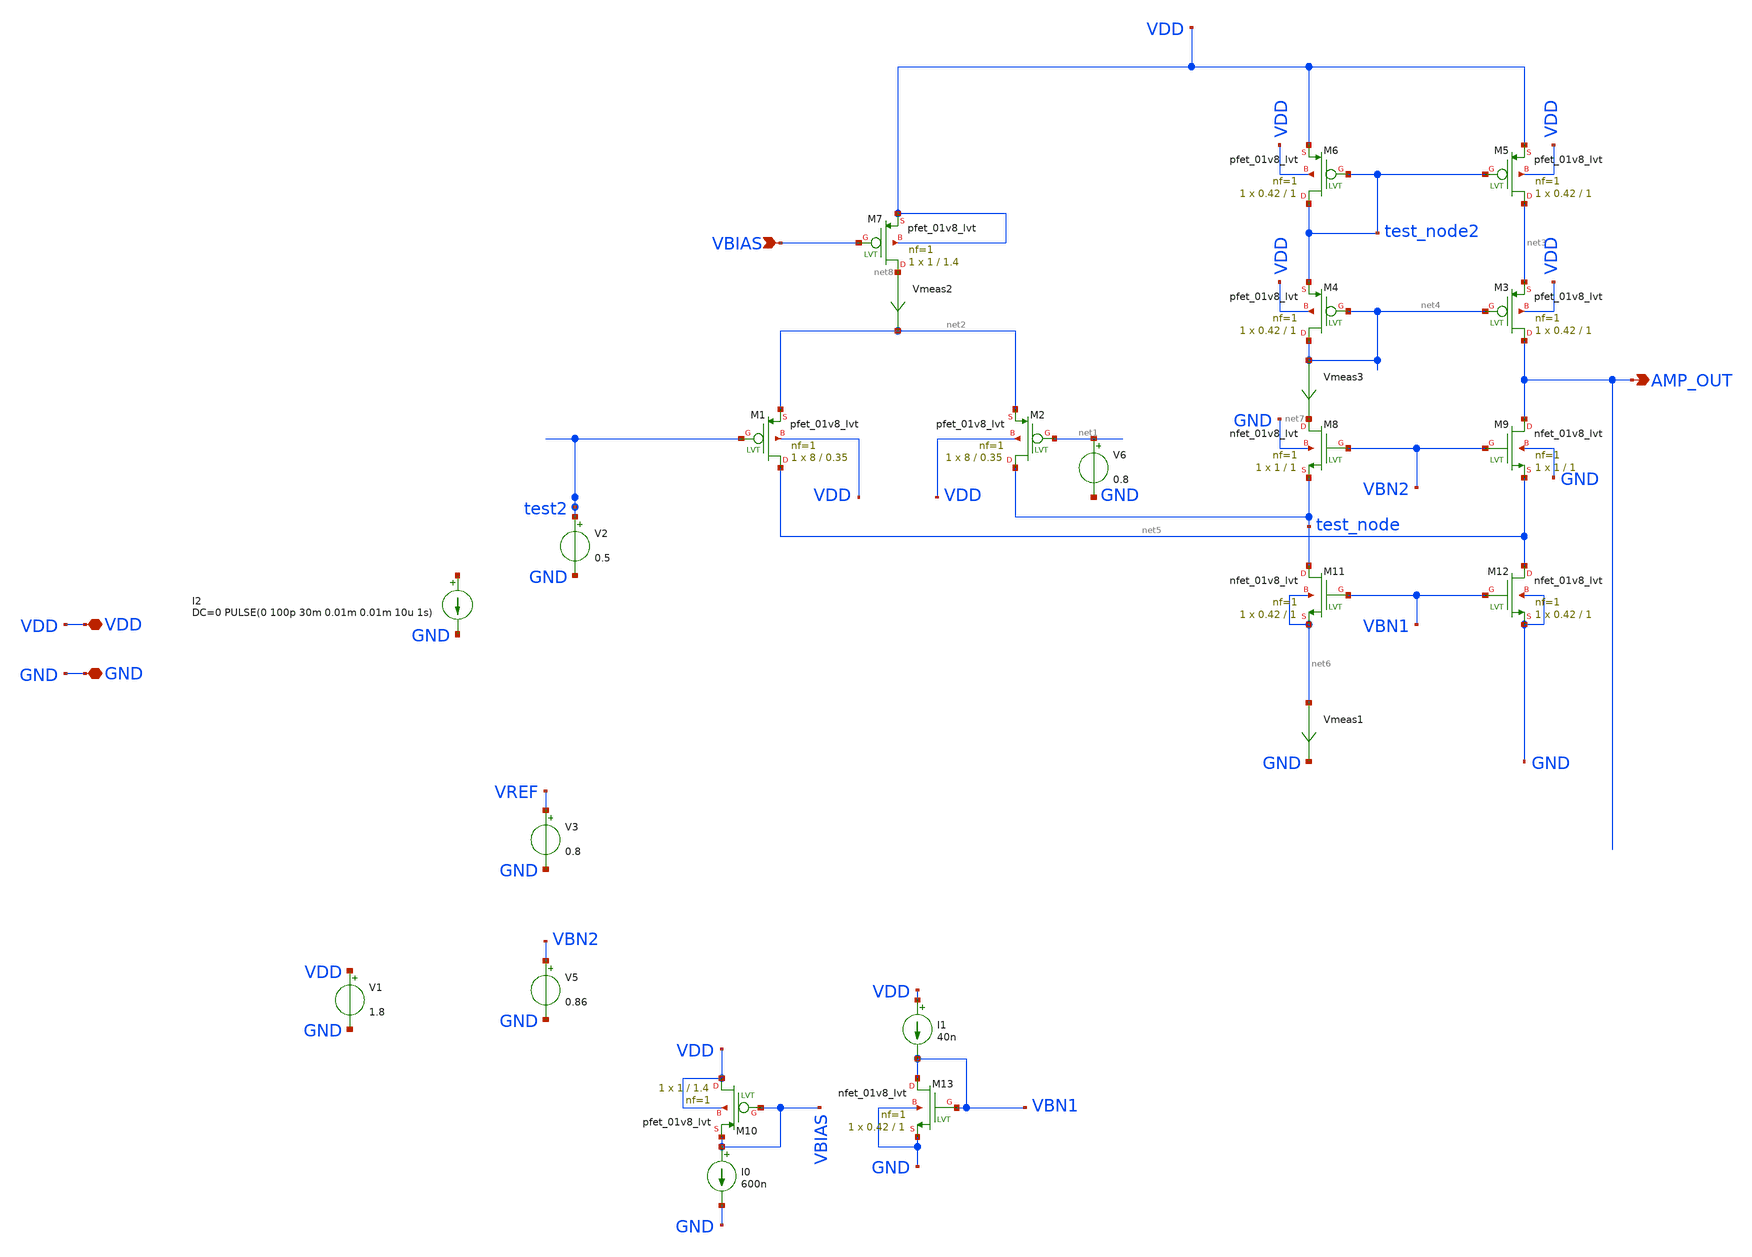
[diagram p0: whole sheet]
** sch_path: xschem/testbench/pmos_fcs.sch
**.subckt pmos_fcs AMP_OUT VBIAS VDD GND
*.opin AMP_OUT
*.ipin VBIAS
*.iopin VDD
*.iopin GND
XM1 net5 test2 net2 VDD sky130_fd_pr__pfet_01v8_lvt L=0.35 W=8 nf=1 ad='int((nf+1)/2) * W/nf * 0.29'
+ as='int((nf+2)/2) * W/nf * 0.29' pd='2*int((nf+1)/2) * (W/nf + 0.29)' ps='2*int((nf+2)/2) * (W/nf + 0.29)'
+ nrd='0.29 / W' nrs='0.29 / W' sa=0 sb=0 sd=0 mult=1 m=1
XM2 test_node net1 net2 VDD sky130_fd_pr__pfet_01v8_lvt L=0.35 W=8 nf=1 ad='int((nf+1)/2) * W/nf * 0.29'
+ as='int((nf+2)/2) * W/nf * 0.29' pd='2*int((nf+1)/2) * (W/nf + 0.29)' ps='2*int((nf+2)/2) * (W/nf + 0.29)'
+ nrd='0.29 / W' nrs='0.29 / W' sa=0 sb=0 sd=0 mult=1 m=1
XM5 net3 test_node2 VDD VDD sky130_fd_pr__pfet_01v8_lvt L=1 W=0.42 nf=1 ad='int((nf+1)/2) * W/nf * 0.29'
+ as='int((nf+2)/2) * W/nf * 0.29' pd='2*int((nf+1)/2) * (W/nf + 0.29)' ps='2*int((nf+2)/2) * (W/nf + 0.29)'
+ nrd='0.29 / W' nrs='0.29 / W' sa=0 sb=0 sd=0 mult=1 m=1
XM6 test_node2 test_node2 VDD VDD sky130_fd_pr__pfet_01v8_lvt L=1 W=0.42 nf=1 ad='int((nf+1)/2) * W/nf * 0.29'
+ as='int((nf+2)/2) * W/nf * 0.29' pd='2*int((nf+1)/2) * (W/nf + 0.29)' ps='2*int((nf+2)/2) * (W/nf + 0.29)'
+ nrd='0.29 / W' nrs='0.29 / W' sa=0 sb=0 sd=0 mult=1 m=1
XM3 AMP_OUT net4 net3 VDD sky130_fd_pr__pfet_01v8_lvt L=1 W=0.42 nf=1 ad='int((nf+1)/2) * W/nf * 0.29'
+ as='int((nf+2)/2) * W/nf * 0.29' pd='2*int((nf+1)/2) * (W/nf + 0.29)' ps='2*int((nf+2)/2) * (W/nf + 0.29)'
+ nrd='0.29 / W' nrs='0.29 / W' sa=0 sb=0 sd=0 mult=1 m=1
XM4 net4 net4 test_node2 VDD sky130_fd_pr__pfet_01v8_lvt L=1 W=0.42 nf=1 ad='int((nf+1)/2) * W/nf * 0.29'
+ as='int((nf+2)/2) * W/nf * 0.29' pd='2*int((nf+1)/2) * (W/nf + 0.29)' ps='2*int((nf+2)/2) * (W/nf + 0.29)'
+ nrd='0.29 / W' nrs='0.29 / W' sa=0 sb=0 sd=0 mult=1 m=1
XM8 net7 VBN2 test_node GND sky130_fd_pr__nfet_01v8_lvt L=1 W=1 nf=1 ad='int((nf+1)/2) * W/nf * 0.29'
+ as='int((nf+2)/2) * W/nf * 0.29' pd='2*int((nf+1)/2) * (W/nf + 0.29)' ps='2*int((nf+2)/2) * (W/nf + 0.29)'
+ nrd='0.29 / W' nrs='0.29 / W' sa=0 sb=0 sd=0 mult=1 m=1
XM9 AMP_OUT VBN2 net5 GND sky130_fd_pr__nfet_01v8_lvt L=1 W=1 nf=1 ad='int((nf+1)/2) * W/nf * 0.29' as='int((nf+2)/2) * W/nf * 0.29'
+ pd='2*int((nf+1)/2) * (W/nf + 0.29)' ps='2*int((nf+2)/2) * (W/nf + 0.29)' nrd='0.29 / W' nrs='0.29 / W'
+ sa=0 sb=0 sd=0 mult=1 m=1
XM7 net8 VBIAS VDD VDD sky130_fd_pr__pfet_01v8_lvt L=1.4 W=1 nf=1 ad='int((nf+1)/2) * W/nf * 0.29' as='int((nf+2)/2) * W/nf * 0.29'
+ pd='2*int((nf+1)/2) * (W/nf + 0.29)' ps='2*int((nf+2)/2) * (W/nf + 0.29)' nrd='0.29 / W' nrs='0.29 / W'
+ sa=0 sb=0 sd=0 mult=1 m=1
XM11 test_node VBN1 net6 net6 sky130_fd_pr__nfet_01v8_lvt L=1 W=0.42 nf=1 ad='int((nf+1)/2) * W/nf * 0.29'
+ as='int((nf+2)/2) * W/nf * 0.29' pd='2*int((nf+1)/2) * (W/nf + 0.29)' ps='2*int((nf+2)/2) * (W/nf + 0.29)'
+ nrd='0.29 / W' nrs='0.29 / W' sa=0 sb=0 sd=0 mult=1 m=1
XM12 net5 VBN1 GND GND sky130_fd_pr__nfet_01v8_lvt L=1 W=0.42 nf=1 ad='int((nf+1)/2) * W/nf * 0.29' as='int((nf+2)/2) * W/nf * 0.29'
+ pd='2*int((nf+1)/2) * (W/nf + 0.29)' ps='2*int((nf+2)/2) * (W/nf + 0.29)' nrd='0.29 / W' nrs='0.29 / W'
+ sa=0 sb=0 sd=0 mult=1 m=1
V2 test2 GND 0.5
V3 VREF GND 0.8
V5 VBN2 GND 0.86
XM10 VDD VBIAS VBIAS VDD sky130_fd_pr__pfet_01v8_lvt L=1.4 W=1 nf=1 ad='int((nf+1)/2) * W/nf * 0.29'
+ as='int((nf+2)/2) * W/nf * 0.29' pd='2*int((nf+1)/2) * (W/nf + 0.29)' ps='2*int((nf+2)/2) * (W/nf + 0.29)'
+ nrd='0.29 / W' nrs='0.29 / W' sa=0 sb=0 sd=0 mult=1 m=1
V1 VDD GND 1.8
I0 VBIAS GND 600n
XM13 VBN1 VBN1 GND GND sky130_fd_pr__nfet_01v8_lvt L=1 W=0.42 nf=1 ad='int((nf+1)/2) * W/nf * 0.29' as='int((nf+2)/2) * W/nf * 0.29'
+ pd='2*int((nf+1)/2) * (W/nf + 0.29)' ps='2*int((nf+2)/2) * (W/nf + 0.29)' nrd='0.29 / W' nrs='0.29 / W'
+ sa=0 sb=0 sd=0 mult=1 m=1
I1 VDD VBN1 40n
Vmeas1 net6 GND 0
.save i(vmeas1)
Vmeas2 net8 net2 0
.save i(vmeas2)
V6 net1 GND 0.8
Vmeas3 net4 net7 0
.save i(vmeas3)
I2 net9 GND DC=0 PULSE(0 100p 30m 0.01m 0.01m 10u 1s)
**** begin user architecture code

** opencircuitdesign pdks install
.lib $::SKYWATER_MODELS/sky130.lib.spice tt


**** end user architecture code
**.ends
**** begin user architecture code


.options gmin=0.0000000000000000000001
*.options savecurrents

.control
save all

*tran 1m 50m
*plot v(test)
*op
dc v2 0.5 1.4 0.0001
*ac dec 10 1 1000Meg
*plot vdb(AMP_OUT) 180*cph(v(AMP_OUT))/pi xlog

*plot v(AMP_OUT)
*plot deriv(v(AMP_OUT))

*noise v(AMP_OUT) V4 dec 10 1 1Meg
*setplot noise2
*print onoise_total

*noise v(PIX_OUT) V8 dec 10 1 1Meg
*setplot noise2
*print onoise_total
.endc


**** end user architecture code
.end
